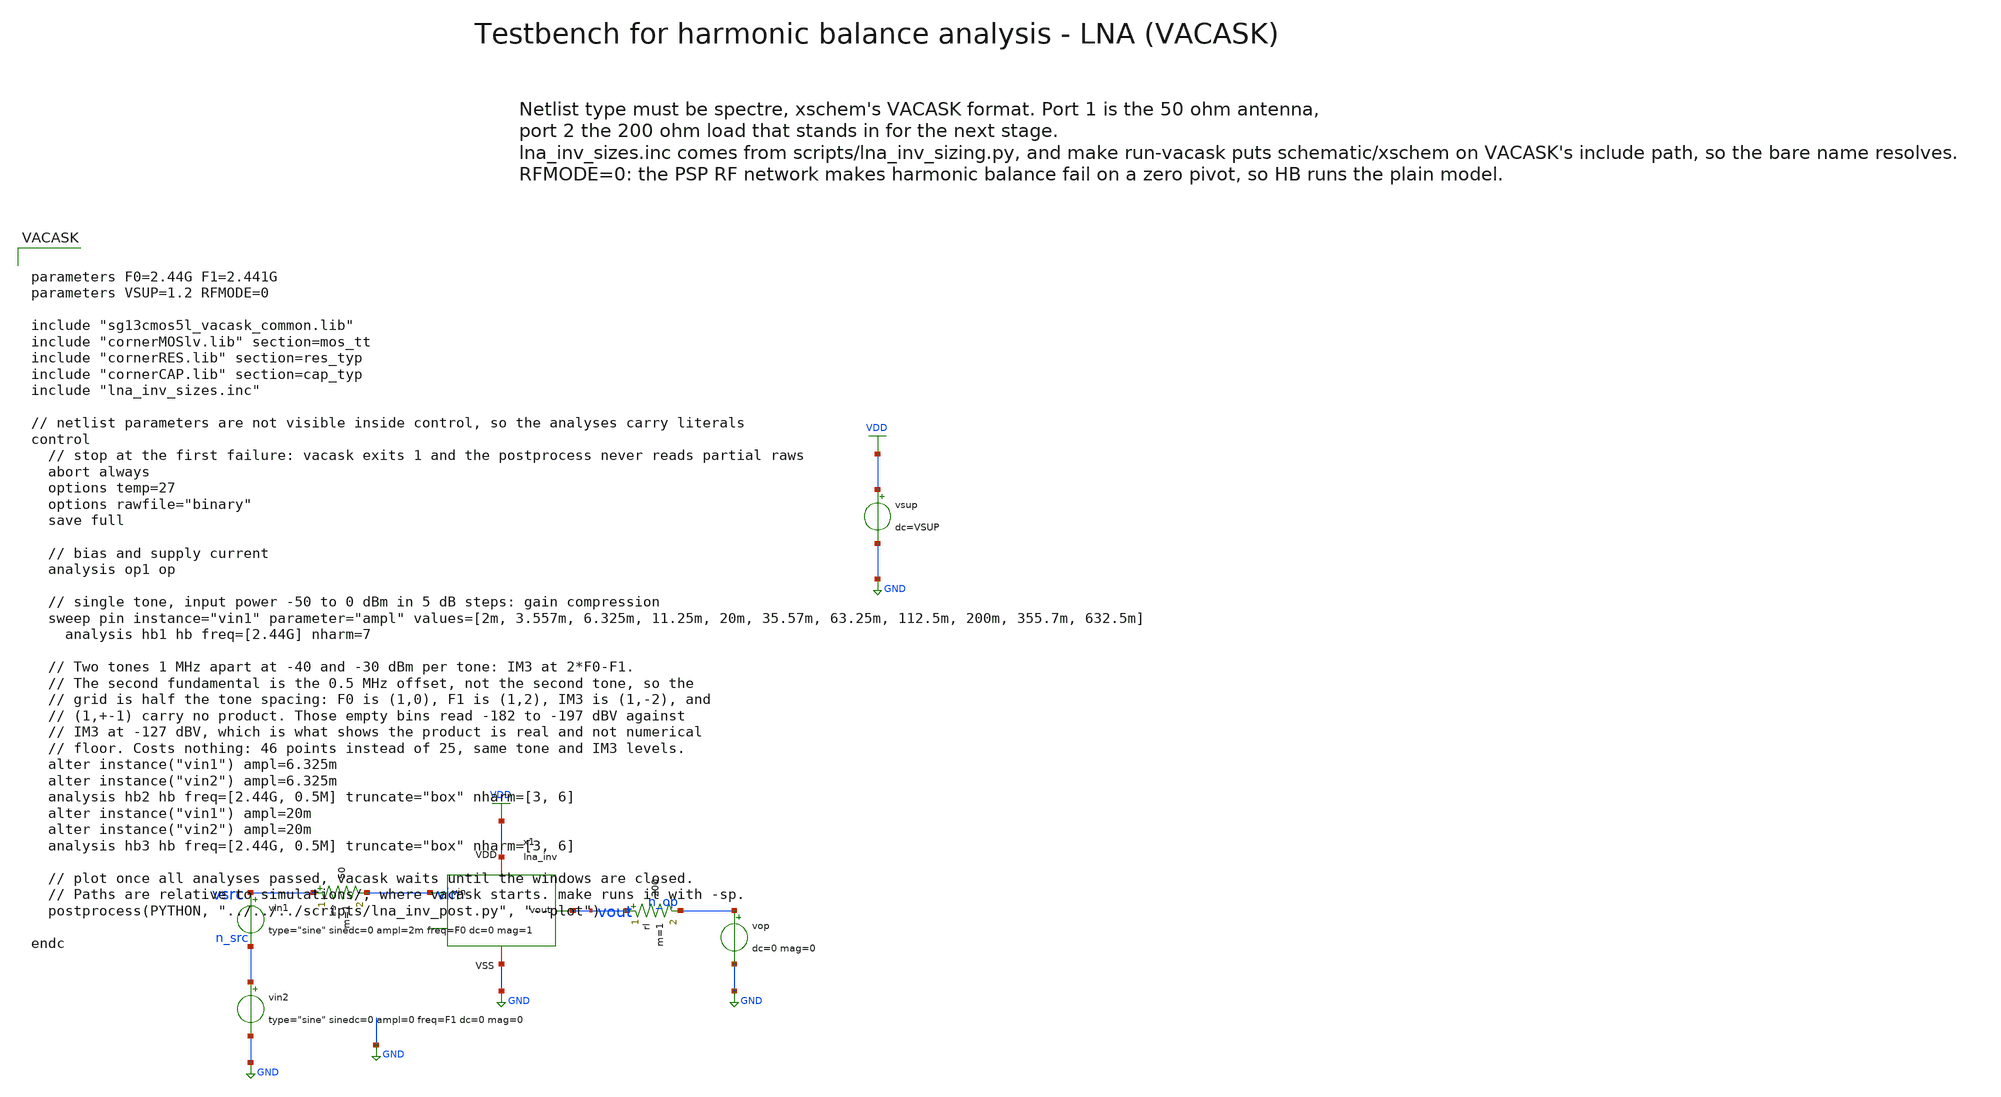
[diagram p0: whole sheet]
** sch_path: macros/lna_inv/testbenches/xschem/lna_inv_tb_hb.sch
**.subckt lna_inv_tb_hb
vin1 vsrc n_src type="sine" sinedc=0 ampl=2m freq=F0 dc=0 mag=1
vin2 n_src GND type="sine" sinedc=0 ampl=0 freq=F1 dc=0 mag=0
rs vsrc vin 50 m=1
x1 vin vout VDD GND lna_inv
rl vout n_op 200 m=1
vop n_op GND dc=0 mag=0
vsup VDD GND dc=VSUP
**** begin user architecture code


parameters F0=2.44G F1=2.441G
parameters VSUP=1.2 RFMODE=0

include "sg13cmos5l_vacask_common.lib"
include "cornerMOSlv.lib" section=mos_tt
include "cornerRES.lib" section=res_typ
include "cornerCAP.lib" section=cap_typ
include "lna_inv_sizes.inc"

// netlist parameters are not visible inside control, so the analyses carry literals
control
  // stop at the first failure: vacask exits 1 and the postprocess never reads partial raws
  abort always
  options temp=27
  options rawfile="binary"
  save full

  // bias and supply current
  analysis op1 op

  // single tone, input power -50 to 0 dBm in 5 dB steps: gain compression
  sweep pin instance="vin1" parameter="ampl" values=[2m, 3.557m, 6.325m, 11.25m, 20m, 35.57m,
+ 63.25m, 112.5m, 200m, 355.7m, 632.5m]
    analysis hb1 hb freq=[2.44G] nharm=7

  // Two tones 1 MHz apart at -40 and -30 dBm per tone: IM3 at 2*F0-F1.
  // The second fundamental is the 0.5 MHz offset, not the second tone, so the
  // grid is half the tone spacing: F0 is (1,0), F1 is (1,2), IM3 is (1,-2), and
  // (1,+-1) carry no product. Those empty bins read -182 to -197 dBV against
  // IM3 at -127 dBV, which is what shows the product is real and not numerical
  // floor. Costs nothing: 46 points instead of 25, same tone and IM3 levels.
  alter instance("vin1") ampl=6.325m
  alter instance("vin2") ampl=6.325m
  analysis hb2 hb freq=[2.44G, 0.5M] truncate="box" nharm=[3, 6]
  alter instance("vin1") ampl=20m
  alter instance("vin2") ampl=20m
  analysis hb3 hb freq=[2.44G, 0.5M] truncate="box" nharm=[3, 6]

  // plot once all analyses passed, vacask waits until the windows are closed.
  // Paths are relative to simulations/, where vacask starts. make runs it with -sp.
  postprocess(PYTHON, "../../../scripts/lna_inv_post.py", "--plot")

endc


**** end user architecture code
**.ends
.GLOBAL GND
.GLOBAL VDD
.end
